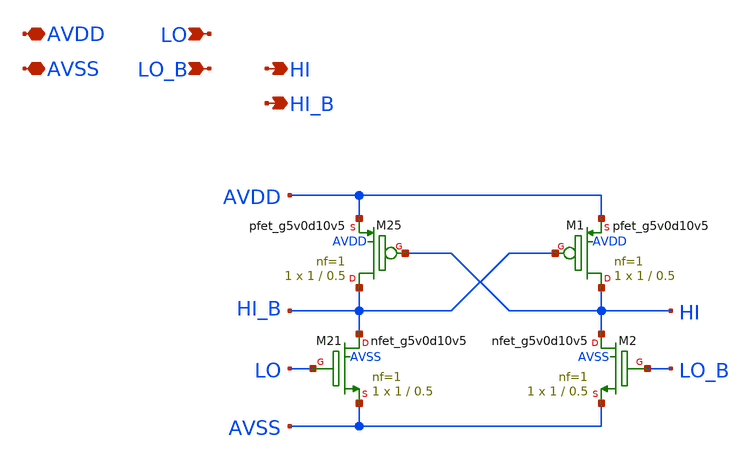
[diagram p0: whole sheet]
** sch_path: xschem/level_shifter_ad.sch
**.subckt level_shifter_ad AVDD AVSS LO HI HI_B LO_B
*.iopin AVDD
*.iopin AVSS
*.ipin LO
*.opin HI
*.opin HI_B
*.ipin LO_B
XM21 HI_B LO AVSS AVSS sky130_fd_pr__nfet_g5v0d10v5 L=0.5 W=1 nf=1 ad='int((nf+1)/2) * W/nf * 0.29' as='int((nf+2)/2) * W/nf * 0.29'
+ pd='2*int((nf+1)/2) * (W/nf + 0.29)' ps='2*int((nf+2)/2) * (W/nf + 0.29)' nrd='0.29 / W' nrs='0.29 / W'
+ sa=0 sb=0 sd=0 mult=1 m=1
XM25 HI_B HI AVDD AVDD sky130_fd_pr__pfet_g5v0d10v5 L=0.5 W=1 nf=1 ad='int((nf+1)/2) * W/nf * 0.29' as='int((nf+2)/2) * W/nf * 0.29'
+ pd='2*int((nf+1)/2) * (W/nf + 0.29)' ps='2*int((nf+2)/2) * (W/nf + 0.29)' nrd='0.29 / W' nrs='0.29 / W'
+ sa=0 sb=0 sd=0 mult=1 m=1
XM1 HI HI_B AVDD AVDD sky130_fd_pr__pfet_g5v0d10v5 L=0.5 W=1 nf=1 ad='int((nf+1)/2) * W/nf * 0.29' as='int((nf+2)/2) * W/nf * 0.29'
+ pd='2*int((nf+1)/2) * (W/nf + 0.29)' ps='2*int((nf+2)/2) * (W/nf + 0.29)' nrd='0.29 / W' nrs='0.29 / W'
+ sa=0 sb=0 sd=0 mult=1 m=1
XM2 HI LO_B AVSS AVSS sky130_fd_pr__nfet_g5v0d10v5 L=0.5 W=1 nf=1 ad='int((nf+1)/2) * W/nf * 0.29' as='int((nf+2)/2) * W/nf * 0.29'
+ pd='2*int((nf+1)/2) * (W/nf + 0.29)' ps='2*int((nf+2)/2) * (W/nf + 0.29)' nrd='0.29 / W' nrs='0.29 / W'
+ sa=0 sb=0 sd=0 mult=1 m=1
**.ends
.end
